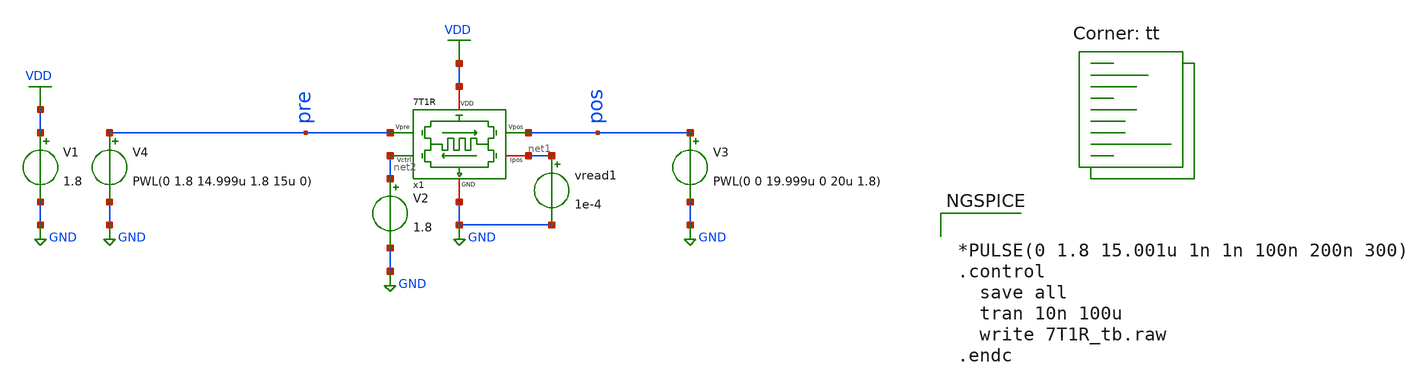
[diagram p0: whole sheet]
** sch_path: synapse/7T1R_tb.sch
**.subckt 7T1R_tb
V1 VDD GND 1.8
V3 pos GND PWL(0 0 19.999u 0 20u 1.8)
vread1 net1 GND 1e-4
V4 pre GND PWL(0 1.8 14.999u 1.8 15u 0)
x1 net2 VDD net1 pre pos GND 7T1R
V2 net2 GND 1.8
**** begin user architecture code
.lib $::SKYWATER_MODELS/sky130.lib.spice tt

** opencircuitdesign pdks install
.inc $::SKYWATER_MODELS/rram_v0.spice



*PULSE(0 1.8 15.001u 1n 1n 100n 200n 300)
.control
  save all
  tran 10n 100u
  write 7T1R_tb.raw
.endc


**** end user architecture code
**.ends

* expanding   symbol:  /home/ricardo/RATT_repos/Proyectos_xschem/synapse/7T1R.sym # of pins=6
** sym_path: synapse/7T1R.sym
** sch_path: synapse/7T1R.sch
.subckt 7T1R Vctrl VDD Ipos Vpre Vpos GND
*.ipin Vpre
*.ipin Vpos
*.iopin GND
*.iopin Ipos
*.iopin VDD
*.ipin Vctrl
XM1 vipre Vpre BE GND sky130_fd_pr__nfet_01v8 L=0.15 W=1 nf=1 ad='int((nf+1)/2) * W/nf * 0.29' as='int((nf+2)/2) * W/nf * 0.29'
+ pd='2*int((nf+1)/2) * (W/nf + 0.29)' ps='2*int((nf+2)/2) * (W/nf + 0.29)' nrd='0.29 / W' nrs='0.29 / W'
+ sa=0 sb=0 sd=0 mult=1 m=1
XR1 TE BE rram_v0
XM3 vipre Vpos TE GND sky130_fd_pr__nfet_01v8 L=0.15 W=20 nf=1 ad='int((nf+1)/2) * W/nf * 0.29' as='int((nf+2)/2) * W/nf * 0.29'
+ pd='2*int((nf+1)/2) * (W/nf + 0.29)' ps='2*int((nf+2)/2) * (W/nf + 0.29)' nrd='0.29 / W' nrs='0.29 / W'
+ sa=0 sb=0 sd=0 mult=1 m=1
XM6 Ipos vipre net1 net1 sky130_fd_pr__pfet_01v8 L=0.15 W=20 nf=1 ad='int((nf+1)/2) * W/nf * 0.29' as='int((nf+2)/2) * W/nf * 0.29'
+ pd='2*int((nf+1)/2) * (W/nf + 0.29)' ps='2*int((nf+2)/2) * (W/nf + 0.29)' nrd='0.29 / W' nrs='0.29 / W'
+ sa=0 sb=0 sd=0 mult=1 m=1
XM5 vipre vipre net1 net1 sky130_fd_pr__pfet_01v8 L=0.15 W=20 nf=1 ad='int((nf+1)/2) * W/nf * 0.29' as='int((nf+2)/2) * W/nf * 0.29'
+ pd='2*int((nf+1)/2) * (W/nf + 0.29)' ps='2*int((nf+2)/2) * (W/nf + 0.29)' nrd='0.29 / W' nrs='0.29 / W'
+ sa=0 sb=0 sd=0 mult=1 m=1
XM2 BE Vpos GND GND sky130_fd_pr__nfet_01v8 L=0.15 W=20 nf=1 ad='int((nf+1)/2) * W/nf * 0.29' as='int((nf+2)/2) * W/nf * 0.29'
+ pd='2*int((nf+1)/2) * (W/nf + 0.29)' ps='2*int((nf+2)/2) * (W/nf + 0.29)' nrd='0.29 / W' nrs='0.29 / W'
+ sa=0 sb=0 sd=0 mult=1 m=1
XM4 TE Vpre GND GND sky130_fd_pr__nfet_01v8 L=0.15 W=1 nf=1 ad='int((nf+1)/2) * W/nf * 0.29' as='int((nf+2)/2) * W/nf * 0.29'
+ pd='2*int((nf+1)/2) * (W/nf + 0.29)' ps='2*int((nf+2)/2) * (W/nf + 0.29)' nrd='0.29 / W' nrs='0.29 / W'
+ sa=0 sb=0 sd=0 mult=1 m=1
XM7 VDD Vctrl net1 GND sky130_fd_pr__nfet_01v8 L=0.15 W=20 nf=1 ad='int((nf+1)/2) * W/nf * 0.29' as='int((nf+2)/2) * W/nf * 0.29'
+ pd='2*int((nf+1)/2) * (W/nf + 0.29)' ps='2*int((nf+2)/2) * (W/nf + 0.29)' nrd='0.29 / W' nrs='0.29 / W'
+ sa=0 sb=0 sd=0 mult=1 m=1
.ends

.GLOBAL GND
.GLOBAL VDD
.end
